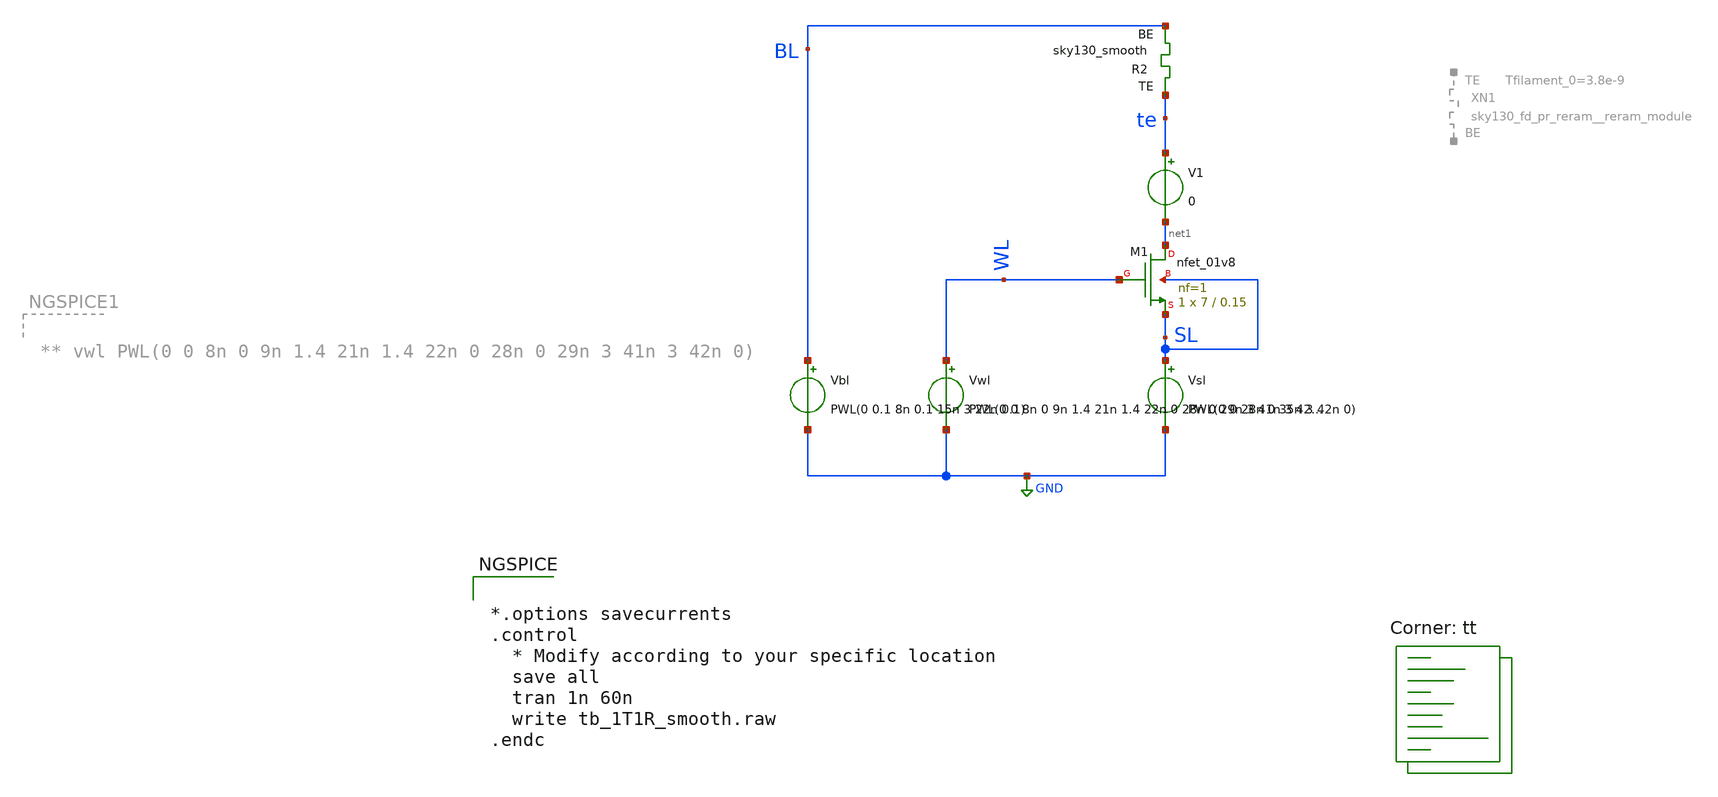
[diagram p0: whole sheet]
** sch_path: memristor_models/sky130_smooth/tb_1T1R_smooth.sch
**.subckt tb_1T1R_smooth
XM1 net1 WL SL SL sky130_fd_pr__nfet_01v8 L=0.15 W=7 nf=1 ad='int((nf+1)/2) * W/nf * 0.29' as='int((nf+2)/2) * W/nf * 0.29'
+ pd='2*int((nf+1)/2) * (W/nf + 0.29)' ps='2*int((nf+2)/2) * (W/nf + 0.29)' nrd='0.29 / W' nrs='0.29 / W'
+ sa=0 sb=0 sd=0 mult=1 m=1
Vwl WL GND PWL(0 0 8n 0 9n 1.4 21n 1.4 22n 0 28n 0 29n 3 41n 3 42n 0)
Vbl BL GND PWL(0 0.1 8n 0.1 15n 3 22n 0.1)
V1 te net1 0
Vsl SL GND PWL(0 0 28n 0 35n 3 42n 0)
XR2 te BL sky130_smooth Tfilament_0=3.3e-9
**** begin user architecture code


*.options savecurrents
.control
  * Modify according to your specific location
  save all
  tran 1n 60n
  write tb_1T1R_smooth.raw
.endc



.lib $::SKYWATER_MODELS/sky130.lib.spice tt

** opencircuitdesign pdks install
.inc $::SKYWATER_MODELS/sky130_smooth.spice

**** end user architecture code
**.ends
.GLOBAL GND
.end
